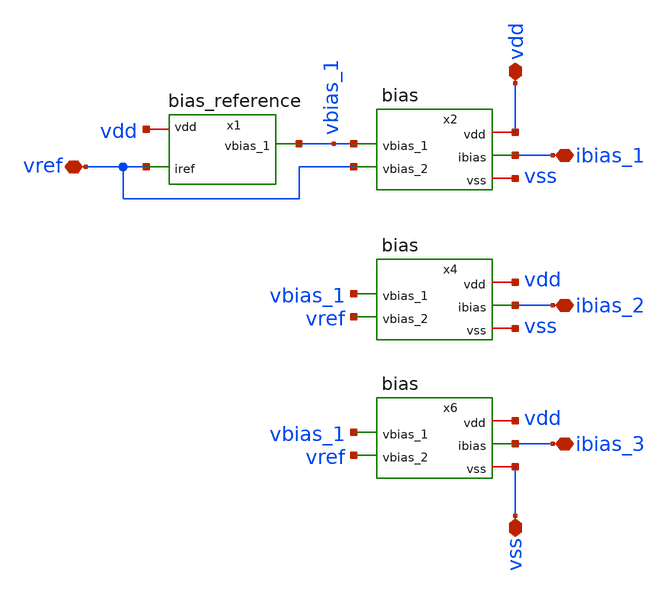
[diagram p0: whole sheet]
** sch_path: track_analogico/bias/sch/bias_circuit.sch
**.subckt bias_circuit ibias_2 vss ibias_1 ibias_3 vdd vref
*.iopin ibias_2
*.iopin vss
*.iopin ibias_1
*.iopin ibias_3
*.iopin vdd
*.iopin vref
x2 vdd vbias_1 vref ibias_1 vss bias
x1 vdd vbias_1 vref bias_reference
x4 vdd vbias_1 vref ibias_2 vss bias
x6 vdd vbias_1 vref ibias_3 vss bias
**.ends
.end
